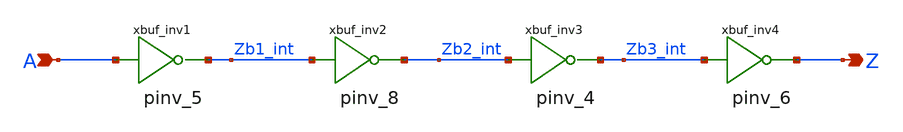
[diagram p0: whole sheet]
** sch_path: sram_2_16_scn4m/pdriver_1.sch
**.subckt pdriver_1 A Z
*.ipin A
*.opin Z
xbuf_inv1 A Zb1_int vdd gnd pinv_5
xbuf_inv2 Zb1_int Zb2_int vdd gnd pinv_8
xbuf_inv3 Zb2_int Zb3_int vdd gnd pinv_4
xbuf_inv4 Zb3_int Z vdd gnd pinv_6
**.ends

* expanding   symbol:  pinv_5.sym # of pins=2
** sym_path: sram_2_16_scn4m/pinv_5.sym
** sch_path: sram_2_16_scn4m/pinv_5.sch
.subckt pinv_5 A Z vdd gnd
*.ipin A
*.opin Z
XMpinv_nmos Z A gnd gnd sky130_fd_pr__nfet_01v8 L=0.4 W=0.8 nf=1 ad='int((nf+1)/2) * W/nf * 0.29' as='int((nf+2)/2) * W/nf * 0.29'
+ pd='2*int((nf+1)/2) * (W/nf + 0.29)' ps='2*int((nf+2)/2) * (W/nf + 0.29)' nrd='0.29 / W' nrs='0.29 / W'
+ sa=0 sb=0 sd=0 mult=1 m=1
XMp_inv_pmos Z A vdd vdd sky130_fd_pr__pfet_01v8 L=0.4 W=1.6 nf=1 ad='int((nf+1)/2) * W/nf * 0.29' as='int((nf+2)/2) * W/nf * 0.29'
+ pd='2*int((nf+1)/2) * (W/nf + 0.29)' ps='2*int((nf+2)/2) * (W/nf + 0.29)' nrd='0.29 / W' nrs='0.29 / W'
+ sa=0 sb=0 sd=0 mult=1 m=1
.ends


* expanding   symbol:  pinv_8.sym # of pins=2
** sym_path: sram_2_64_scn4m/pinv_8.sym
** sch_path: sram_2_64_scn4m/pinv_8.sch
.subckt pinv_8 A Z vdd gnd
*.ipin A
*.opin Z
XMpinv_nmos Z A gnd gnd sky130_fd_pr__nfet_01v8 L=0.4 W=2.8 nf=1 ad='int((nf+1)/2) * W/nf * 0.29' as='int((nf+2)/2) * W/nf * 0.29'
+ pd='2*int((nf+1)/2) * (W/nf + 0.29)' ps='2*int((nf+2)/2) * (W/nf + 0.29)' nrd='0.29 / W' nrs='0.29 / W'
+ sa=0 sb=0 sd=0 mult=1 m=1
XMp_inv_pmos Z A vdd vdd sky130_fd_pr__pfet_01v8 L=0.4 W=5.6 nf=1 ad='int((nf+1)/2) * W/nf * 0.29' as='int((nf+2)/2) * W/nf * 0.29'
+ pd='2*int((nf+1)/2) * (W/nf + 0.29)' ps='2*int((nf+2)/2) * (W/nf + 0.29)' nrd='0.29 / W' nrs='0.29 / W'
+ sa=0 sb=0 sd=0 mult=1 m=1
.ends


* expanding   symbol:  pinv_4.sym # of pins=2
** sym_path: sram_2_64_scn4m/pinv_4.sym
** sch_path: sram_2_64_scn4m/pinv_4.sch
.subckt pinv_4 A Z vdd gnd
*.ipin A
*.opin Z
Mpinv_nmos Z A gnd gnd n w=3.2u l=0.4u m=1
Mp_inv_pmos Z A vdd vdd p w=6.4u l=0.4u m=1
.ends


* expanding   symbol:  pinv_6.sym # of pins=2
** sym_path: sram_2_64_scn4m/pinv_6.sym
** sch_path: sram_2_64_scn4m/pinv_6.sch
.subckt pinv_6 A Z vdd gnd
*.ipin A
*.opin Z
Mpinv_nmos Z A gnd gnd n w=3.2u l=0.4u m=1
Mp_inv_pmos Z A vdd vdd p w=6.4u l=0.4u m=1
.ends

.end
